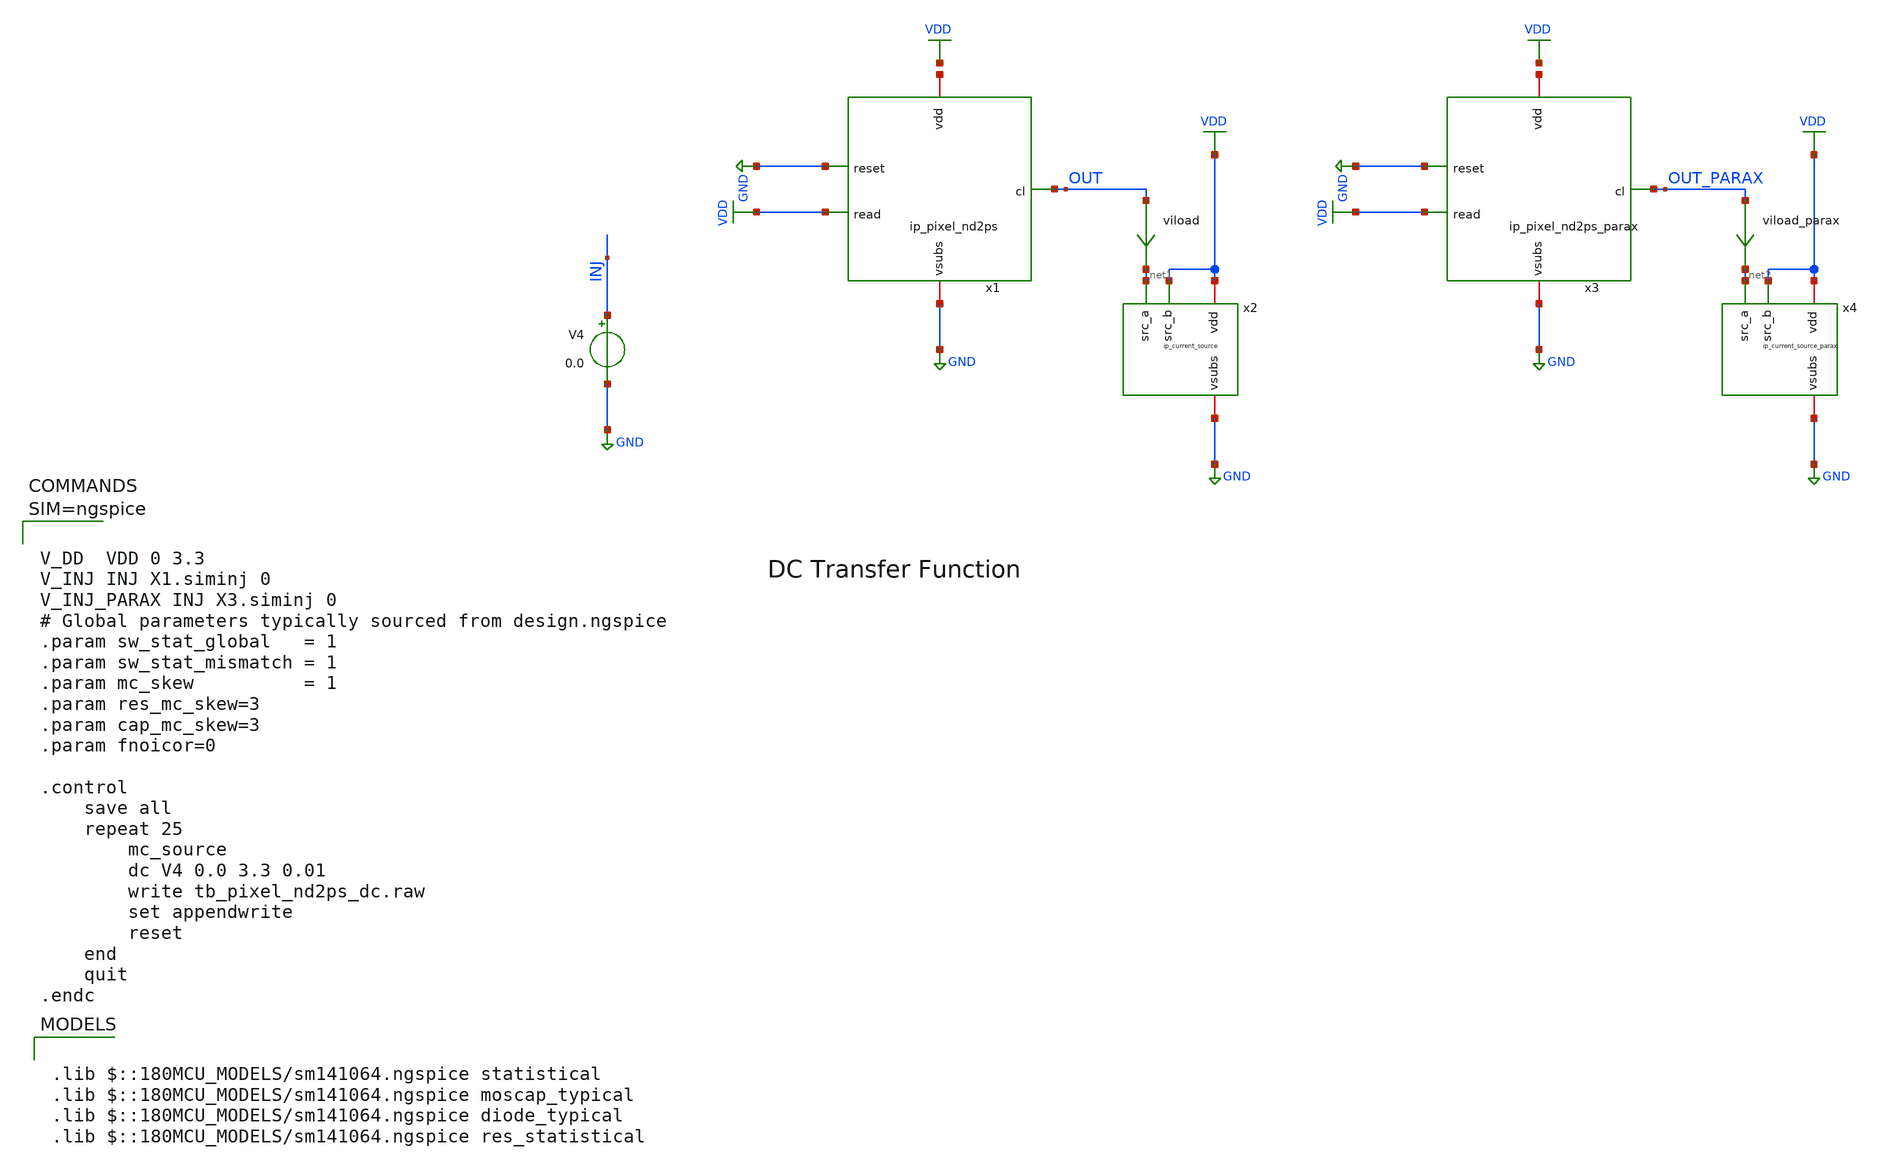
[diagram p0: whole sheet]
** sch_path: xschem/tb_pixel_nd2ps_dc.sch
**.subckt tb_pixel_nd2ps_dc
x1 net3 GND VDD GND OUT ip_pixel_nd2ps
V4 INJ GND 0.0
x2 VDD net1 GND VDD ip_current_source
viload OUT net1 0
x3 net4 GND VDD GND OUT_PARAX ip_pixel_nd2ps_parax
x4 VDD net2 GND VDD ip_current_source_parax
viload_parax OUT_PARAX net2 0
**** begin user architecture code

.lib $::180MCU_MODELS/sm141064.ngspice statistical
.lib $::180MCU_MODELS/sm141064.ngspice moscap_typical
.lib $::180MCU_MODELS/sm141064.ngspice diode_typical
.lib $::180MCU_MODELS/sm141064.ngspice res_statistical




V_DD  VDD 0 3.3
V_INJ INJ X1.siminj 0
V_INJ_PARAX INJ X3.siminj 0
# Global parameters typically sourced from design.ngspice
.param sw_stat_global   = 1
.param sw_stat_mismatch = 1
.param mc_skew          = 1
.param res_mc_skew=3
.param cap_mc_skew=3
.param fnoicor=0

.control
	save all
	repeat 25
		mc_source
		dc V4 0.0 3.3 0.01
		write tb_pixel_nd2ps_dc.raw
		set appendwrite
		reset
	end
	quit
.endc



**** end user architecture code
**.ends

* expanding   symbol:  ip_pixel_nd2ps.sym # of pins=5
** sym_path: xschem/ip_pixel_nd2ps.sym
** sch_path: xschem/ip_pixel_nd2ps.sch
.subckt ip_pixel_nd2ps vdd reset read vsubs cl
*.iopin vdd
*.iopin vsubs
*.ipin reset
*.ipin read
*.opin cl
D2 vsubs siminj diode_nd2ps_06v0 area='13.5u * 13.5u ' pj='2*13.5u + 2*13.5u ' m=1
XM4 vdd siminj sfout vsubs nfet_06v0 L=1.0u W=2.5u nf=1 ad='int((nf+1)/2) * W/nf * 0.18u' as='int((nf+2)/2) * W/nf * 0.18u'
+ pd='2*int((nf+1)/2) * (W/nf + 0.18u)' ps='2*int((nf+2)/2) * (W/nf + 0.18u)' nrd='0.18u / W' nrs='0.18u / W'
+ sa=0 sb=0 sd=0 m=1 par=1
XM2 vdd reset siminj vsubs nfet_06v0 L=0.7u W=0.30u nf=1 ad='int((nf+1)/2) * W/nf * 0.18u' as='int((nf+2)/2) * W/nf * 0.18u'
+ pd='2*int((nf+1)/2) * (W/nf + 0.18u)' ps='2*int((nf+2)/2) * (W/nf + 0.18u)' nrd='0.18u / W' nrs='0.18u / W'
+ sa=0 sb=0 sd=0 m=1 par=1
XM1 sfout read cl vsubs nfet_06v0 L=0.7u W=0.30u nf=1 ad='int((nf+1)/2) * W/nf * 0.18u' as='int((nf+2)/2) * W/nf * 0.18u'
+ pd='2*int((nf+1)/2) * (W/nf + 0.18u)' ps='2*int((nf+2)/2) * (W/nf + 0.18u)' nrd='0.18u / W' nrs='0.18u / W'
+ sa=0 sb=0 sd=0 m=1 par=1
.ends


* expanding   symbol:  ip_current_source.sym # of pins=4
** sym_path: xschem/ip_current_source.sym
** sch_path: xschem/ip_current_source.sch
.subckt ip_current_source vdd src_a vsubs src_b
*.iopin vdd
*.iopin vsubs
*.ipin src_a
*.ipin src_b
XM8 refin refin vsubs vsubs nfet_06v0 L=1u W=5u nf=1 ad='int((nf+1)/2) * W/nf * 0.18u' as='int((nf+2)/2) * W/nf * 0.18u'
+ pd='2*int((nf+1)/2) * (W/nf + 0.18u)' ps='2*int((nf+2)/2) * (W/nf + 0.18u)' nrd='0.18u / W' nrs='0.18u / W'
+ sa=0 sb=0 sd=0 m=1 par=1
XM5 src_a refin net1 vsubs nfet_06v0 L=0.7u W=5u nf=1 ad='int((nf+1)/2) * W/nf * 0.18u' as='int((nf+2)/2) * W/nf * 0.18u'
+ pd='2*int((nf+1)/2) * (W/nf + 0.18u)' ps='2*int((nf+2)/2) * (W/nf + 0.18u)' nrd='0.18u / W' nrs='0.18u / W'
+ sa=0 sb=0 sd=0 m=2 par=2
XM3 src_b refin net2 vsubs nfet_06v0 L=0.7u W=5u nf=1 ad='int((nf+1)/2) * W/nf * 0.18u' as='int((nf+2)/2) * W/nf * 0.18u'
+ pd='2*int((nf+1)/2) * (W/nf + 0.18u)' ps='2*int((nf+2)/2) * (W/nf + 0.18u)' nrd='0.18u / W' nrs='0.18u / W'
+ sa=0 sb=0 sd=0 m=2 par=2
XM4 net1 refin vsubs vsubs nfet_06v0 L=5u W=0.5u nf=1 ad='int((nf+1)/2) * W/nf * 0.18u' as='int((nf+2)/2) * W/nf * 0.18u'
+ pd='2*int((nf+1)/2) * (W/nf + 0.18u)' ps='2*int((nf+2)/2) * (W/nf + 0.18u)' nrd='0.18u / W' nrs='0.18u / W'
+ sa=0 sb=0 sd=0 m=1 par=1
XM7 net2 refin vsubs vsubs nfet_06v0 L=5u W=0.5u nf=1 ad='int((nf+1)/2) * W/nf * 0.18u' as='int((nf+2)/2) * W/nf * 0.18u'
+ pd='2*int((nf+1)/2) * (W/nf + 0.18u)' ps='2*int((nf+2)/2) * (W/nf + 0.18u)' nrd='0.18u / W' nrs='0.18u / W'
+ sa=0 sb=0 sd=0 m=1 par=1
XR5 refin vdd vsubs ppolyf_u_1k_6p0 r_width=1e-6 r_length=42e-6 m=1
.ends


* expanding   symbol:  ip_pixel_nd2ps_parax.sym # of pins=5
** sym_path: xschem/ip_pixel_nd2ps.sym
.include [file normalize ./parax/ip_pixel_nd2ps.sim.spice]

* expanding   symbol:  ip_current_source_parax.sym # of pins=4
** sym_path: xschem/ip_current_source.sym
.include [file normalize ./parax/ip_current_source.sim.spice]
.GLOBAL GND
.GLOBAL VDD
.end
